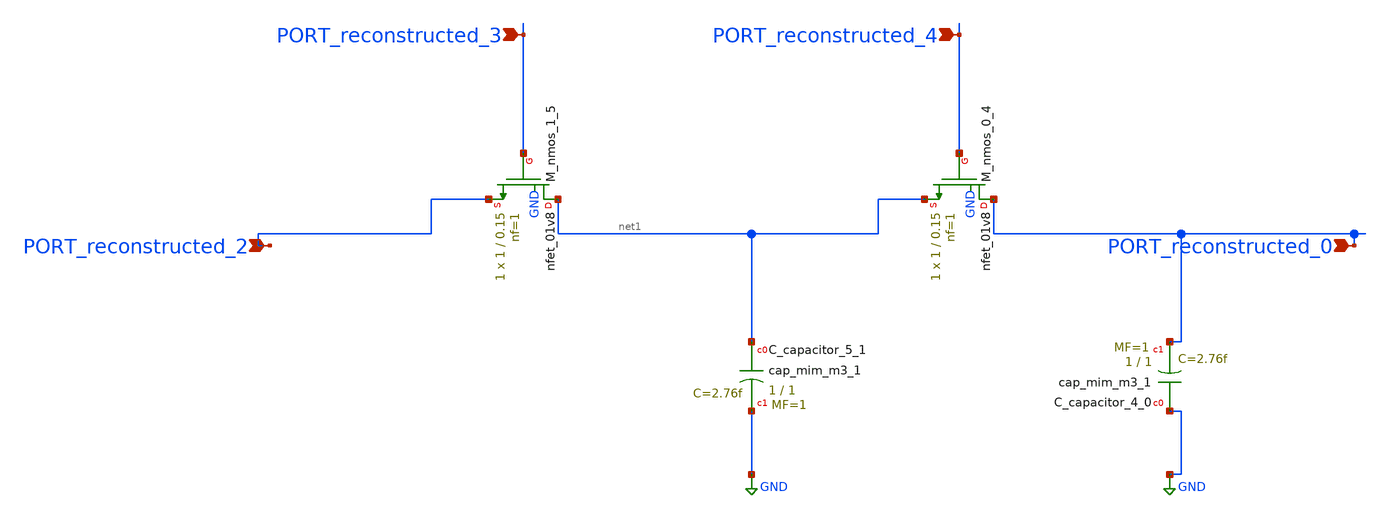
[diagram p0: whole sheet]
** sch_path: schematics/AMSNet/796.sch
**.subckt 796 PORT_reconstructed_2 PORT_reconstructed_0 PORT_reconstructed_4 PORT_reconstructed_3
*.ipin PORT_reconstructed_2
*.ipin PORT_reconstructed_0
*.ipin PORT_reconstructed_4
*.ipin PORT_reconstructed_3
XC_capacitor_4_0 GND PORT_reconstructed_0 sky130_fd_pr__cap_mim_m3_1 W=1 L=1 MF=1 m=1
XC_capacitor_5_1 net1 GND sky130_fd_pr__cap_mim_m3_1 W=1 L=1 MF=1 m=1
XM_nmos_0_4 PORT_reconstructed_0 PORT_reconstructed_4 net1 GND sky130_fd_pr__nfet_01v8 L=0.15 W=1 nf=1
+ ad='int((1 + 1)/2) * 1 / 1 * 0.29' as='int((1 + 2)/2) * 1 / 1 * 0.29' pd='2*int((1 + 1)/2) * (1 / 1 + 0.29)'
+ ps='2*int((1 + 2)/2) * (1 / 1 + 0.29)' nrd='0.29 / 1 ' nrs='0.29 / 1 ' sa=0 sb=0 sd=0 mult=1 m=1
XM_nmos_1_5 net1 PORT_reconstructed_3 PORT_reconstructed_2 GND sky130_fd_pr__nfet_01v8 L=0.15 W=1 nf=1
+ ad='int((1 + 1)/2) * 1 / 1 * 0.29' as='int((1 + 2)/2) * 1 / 1 * 0.29' pd='2*int((1 + 1)/2) * (1 / 1 + 0.29)'
+ ps='2*int((1 + 2)/2) * (1 / 1 + 0.29)' nrd='0.29 / 1 ' nrs='0.29 / 1 ' sa=0 sb=0 sd=0 mult=1 m=1
**.ends
.GLOBAL GND
.end
